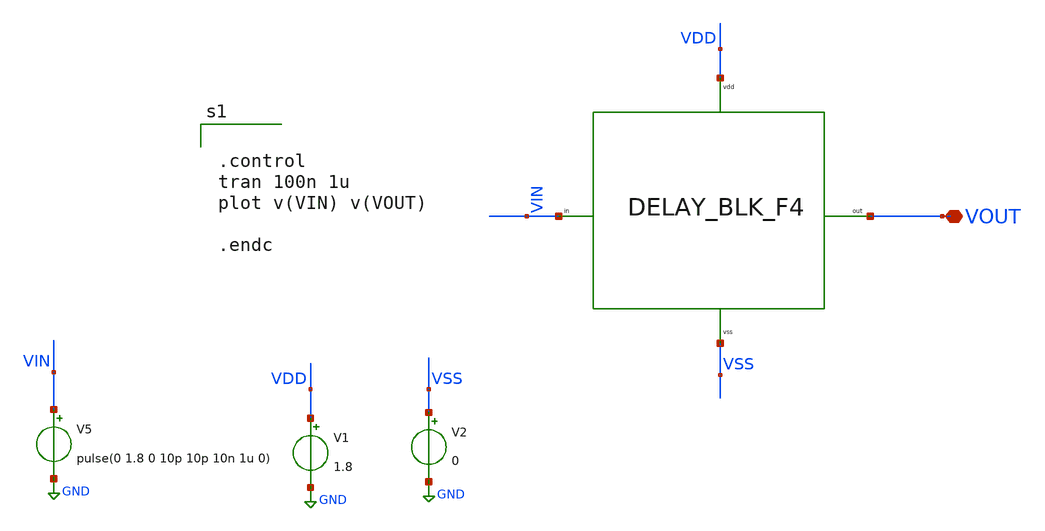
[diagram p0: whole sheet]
** sch_path: xschem/DC_DC_Converter_xschem/OTHERS/DC_DC_Converter_JV10/DELAY_JAWAD/top.sch
**.subckt top VOUT
*.iopin VOUT
V5 VIN GND pulse(0 1.8 0 10p 10p 10n 1u 0)
V1 VDD GND 1.8
V2 VSS GND 0
X1 VIN VOUT VDD VSS Delay_BLK_F4
**** begin user architecture code

** opencircuitdesign pdks install
.lib $::SKYWATER_MODELS/sky130.lib.spice tt




.control
tran 100n 1u
plot v(VIN) v(VOUT)

.endc


**** end user architecture code
**.ends
.GLOBAL GND
.end
